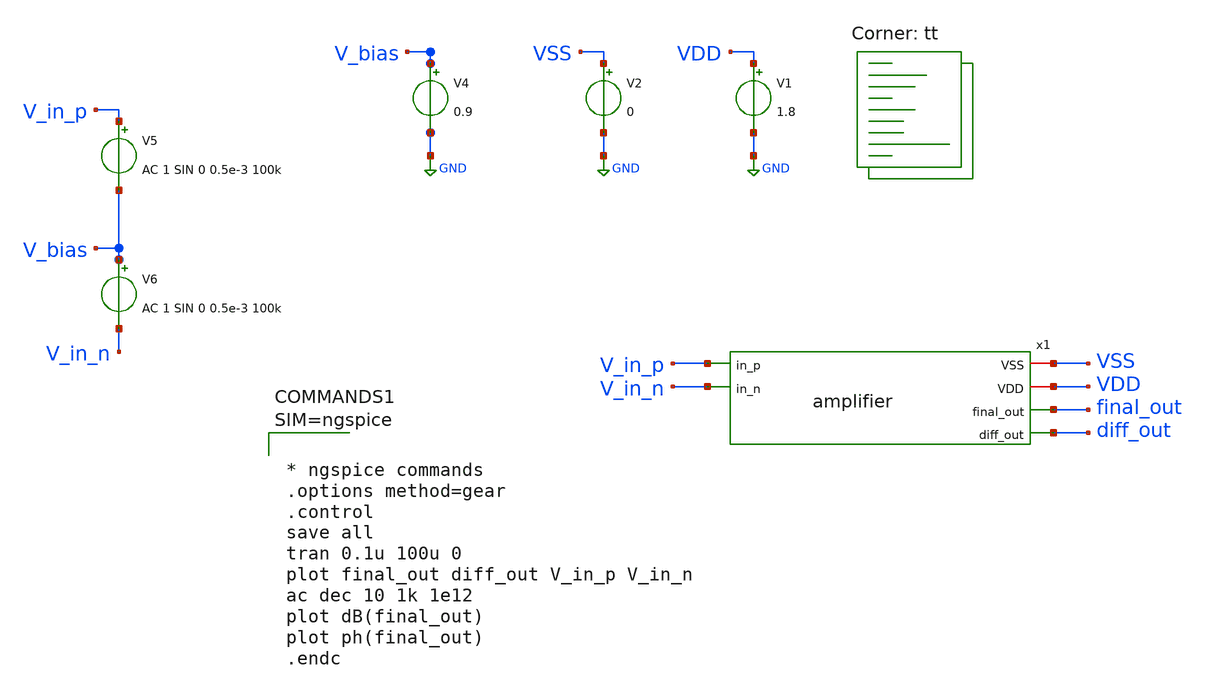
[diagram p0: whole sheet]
** sch_path: xschem/tests/amplifier_test.sch
**.subckt amplifier_test
V1 VDD GND 1.8
V2 VSS GND 0
V4 V_bias GND 0.9
V5 V_in_p V_bias AC 1 SIN 0 0.5e-3 100k
V6 V_bias V_in_n AC 1 SIN 0 0.5e-3 100k
x1 V_in_p V_in_n VSS VDD final_out diff_out amplifier
**** begin user architecture code
.lib $::SKYWATER_MODELS/sky130.lib.spice tt



* ngspice commands
.options method=gear
.control
save all
tran 0.1u 100u 0
plot final_out diff_out V_in_p V_in_n
ac dec 10 1k 1e12
plot dB(final_out)
plot ph(final_out)
.endc



**** end user architecture code
**.ends

* expanding   symbol:  src/amplifier.sym # of pins=6
** sym_path: xschem/src/amplifier.sym
** sch_path: xschem/src/amplifier.sch
.subckt amplifier in_p in_n VSS VDD final_out diff_out
*.ipin in_p
*.iopin VDD
*.ipin in_n
*.iopin VSS
*.opin final_out
*.opin diff_out
XM1 net2 VDD VSS VSS sky130_fd_pr__nfet_01v8 L=0.15 W=30 nf=4 ad='int((nf+1)/2) * W/nf * 0.29' as='int((nf+2)/2) * W/nf * 0.29'
+ pd='2*int((nf+1)/2) * (W/nf + 0.29)' ps='2*int((nf+2)/2) * (W/nf + 0.29)' nrd='0.29 / W' nrs='0.29 / W'
+ sa=0 sb=0 sd=0 mult=1 m=1
XM2 diff_out net1 VDD VDD sky130_fd_pr__pfet_01v8 L=0.15 W=30 nf=4 ad='int((nf+1)/2) * W/nf * 0.29' as='int((nf+2)/2) * W/nf * 0.29'
+ pd='2*int((nf+1)/2) * (W/nf + 0.29)' ps='2*int((nf+2)/2) * (W/nf + 0.29)' nrd='0.29 / W' nrs='0.29 / W'
+ sa=0 sb=0 sd=0 mult=1 m=1
XM3 VDD net1 net1 VDD sky130_fd_pr__pfet_01v8 L=0.15 W=30 nf=4 ad='int((nf+1)/2) * W/nf * 0.29' as='int((nf+2)/2) * W/nf * 0.29'
+ pd='2*int((nf+1)/2) * (W/nf + 0.29)' ps='2*int((nf+2)/2) * (W/nf + 0.29)' nrd='0.29 / W' nrs='0.29 / W'
+ sa=0 sb=0 sd=0 mult=1 m=1
XM4 net1 in_p net2 VSS sky130_fd_pr__nfet_01v8 L=0.15 W=5.7 nf=1 ad='int((nf+1)/2) * W/nf * 0.29' as='int((nf+2)/2) * W/nf * 0.29'
+ pd='2*int((nf+1)/2) * (W/nf + 0.29)' ps='2*int((nf+2)/2) * (W/nf + 0.29)' nrd='0.29 / W' nrs='0.29 / W'
+ sa=0 sb=0 sd=0 mult=1 m=1
XM5 net2 in_n diff_out VSS sky130_fd_pr__nfet_01v8 L=0.15 W=5.7 nf=1 ad='int((nf+1)/2) * W/nf * 0.29'
+ as='int((nf+2)/2) * W/nf * 0.29' pd='2*int((nf+1)/2) * (W/nf + 0.29)' ps='2*int((nf+2)/2) * (W/nf + 0.29)'
+ nrd='0.29 / W' nrs='0.29 / W' sa=0 sb=0 sd=0 mult=1 m=1
XM6 VSS VDD VDD VSS sky130_fd_pr__nfet_01v8 L=.15 W=7.5 nf=1 ad='int((nf+1)/2) * W/nf * 0.29' as='int((nf+2)/2) * W/nf * 0.29'
+ pd='2*int((nf+1)/2) * (W/nf + 0.29)' ps='2*int((nf+2)/2) * (W/nf + 0.29)' nrd='0.29 / W' nrs='0.29 / W'
+ sa=0 sb=0 sd=0 mult=1 m=1
XM7 final_out VDD VSS VSS sky130_fd_pr__nfet_01v8 L=0.15 W=.6 nf=1 ad='int((nf+1)/2) * W/nf * 0.29' as='int((nf+2)/2) * W/nf * 0.29'
+ pd='2*int((nf+1)/2) * (W/nf + 0.29)' ps='2*int((nf+2)/2) * (W/nf + 0.29)' nrd='0.29 / W' nrs='0.29 / W'
+ sa=0 sb=0 sd=0 mult=1 m=1
XM8 final_out diff_out VDD VDD sky130_fd_pr__pfet_01v8 L=0.15 W=30 nf=4 ad='int((nf+1)/2) * W/nf * 0.29'
+ as='int((nf+2)/2) * W/nf * 0.29' pd='2*int((nf+1)/2) * (W/nf + 0.29)' ps='2*int((nf+2)/2) * (W/nf + 0.29)'
+ nrd='0.29 / W' nrs='0.29 / W' sa=0 sb=0 sd=0 mult=1 m=1
.ends

.GLOBAL GND
.end
